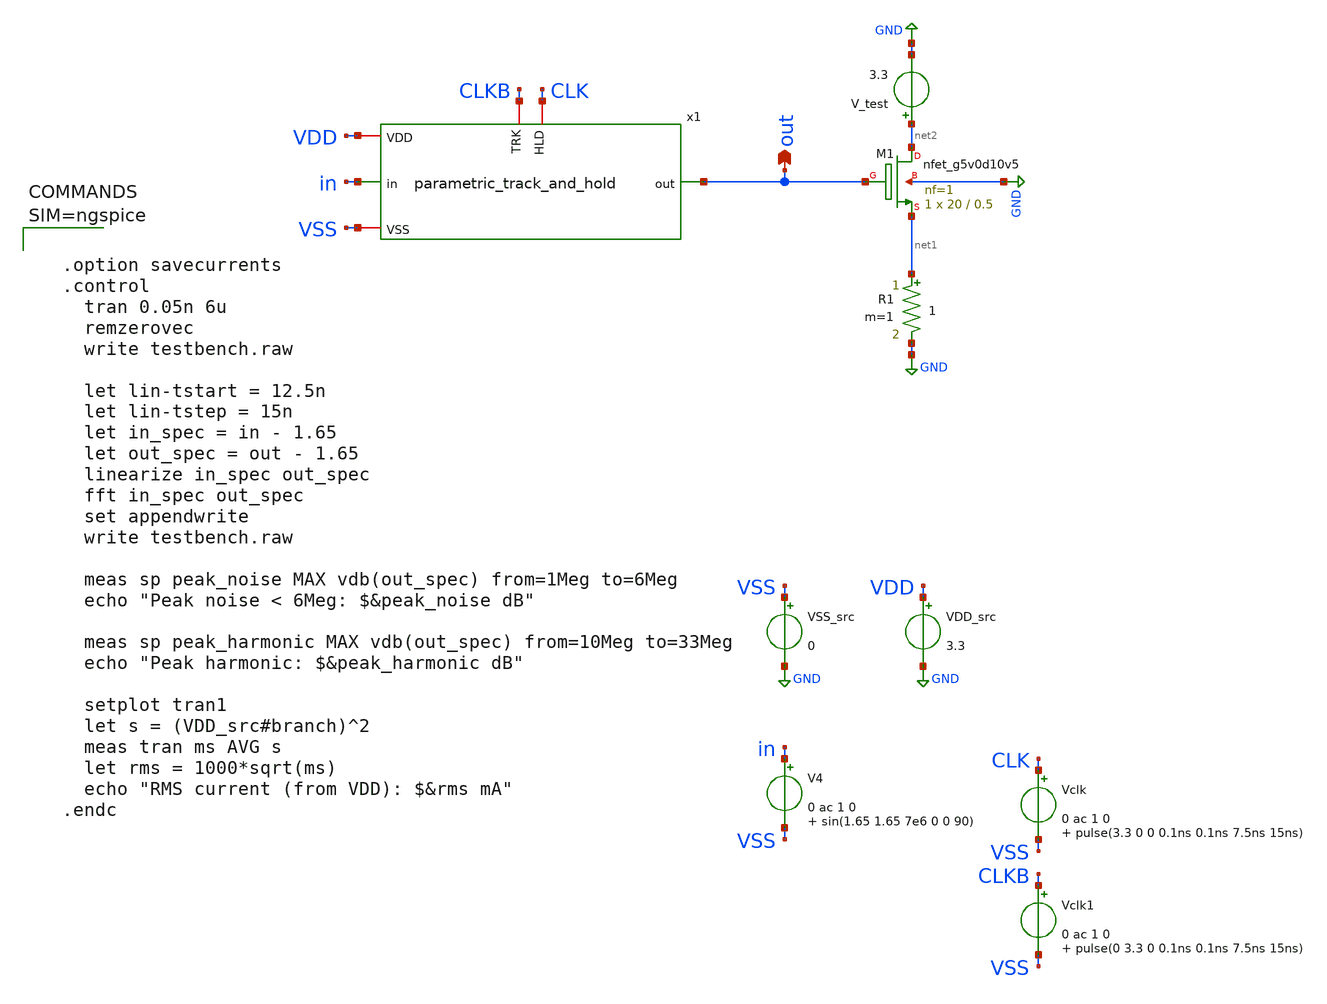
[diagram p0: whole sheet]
** sch_path: xschem/testbench.sch
**.subckt testbench out
*.opin out
VDD_src VDD GND 3.3
VSS_src VSS GND 0
V4 in VSS 0 ac 1 0 sin(1.65 1.65 7e6 0 0 90)
XM1 net2 out net1 GND sky130_fd_pr__nfet_g5v0d10v5 L=0.5 W=20 nf=1 ad='int((nf+1)/2) * W/nf * 0.29' as='int((nf+2)/2) * W/nf * 0.29'
+ pd='2*int((nf+1)/2) * (W/nf + 0.29)' ps='2*int((nf+2)/2) * (W/nf + 0.29)' nrd='0.29 / W' nrs='0.29 / W'
+ sa=0 sb=0 sd=0 mult=1 m=1
R1 net1 GND 1 m=1
Vclk CLK VSS 0 ac 1 0 pulse(3.3 0 0 0.1ns 0.1ns 7.5ns 15ns)
Vclk1 CLKB VSS 0 ac 1 0 pulse(0 3.3 0 0.1ns 0.1ns 7.5ns 15ns)
x1 CLK CLKB VDD VSS out in parametric_track_and_hold WT=1 PFT=1.21 PF=2 WS=5 WB=5 CB=18
V_test net2 GND 3.3
**** begin user architecture code

** opencircuitdesign pdks install
.lib $::SKYWATER_MODELS/sky130.lib.spice tt





  .option savecurrents
  .control
    tran 0.05n 6u
    remzerovec
    write testbench.raw

    let lin-tstart = 12.5n
    let lin-tstep = 15n
    let in_spec = in - 1.65
    let out_spec = out - 1.65
    linearize in_spec out_spec
    fft in_spec out_spec
    set appendwrite
    write testbench.raw

    meas sp peak_noise MAX vdb(out_spec) from=1Meg to=6Meg
    echo "Peak noise < 6Meg: $&peak_noise dB"

    meas sp peak_harmonic MAX vdb(out_spec) from=10Meg to=33Meg
    echo "Peak harmonic: $&peak_harmonic dB"

    setplot tran1
    let s = (VDD_src#branch)^2
    meas tran ms AVG s
    let rms = 1000*sqrt(ms)
    echo "RMS current (from VDD): $&rms mA"
  .endc



**** end user architecture code
**.ends

* expanding   symbol:  parametric_track_and_hold.sym # of pins=6
** sym_path: xschem/parametric_track_and_hold.sym
** sch_path: xschem/parametric_track_and_hold.sch
.subckt parametric_track_and_hold HLD TRK VDD VSS out in  WT=1 PFT=1.21 PF=2 WS=5 WB=5 CB=18
*.iopin VSS
*.iopin VDD
*.ipin in
*.opin out
*.iopin HLD
*.iopin TRK
XC2 out VSS sky130_fd_pr__cap_mim_m3_1 W=5 L=5 MF=1 m=1
XM1 out X in VSS sky130_fd_pr__nfet_g5v0d10v5 L=0.5 W={WT} nf=1 ad='int((nf+1)/2) * W/nf * 0.29' as='int((nf+2)/2) * W/nf * 0.29'
+ pd='2*int((nf+1)/2) * (W/nf + 0.29)' ps='2*int((nf+2)/2) * (W/nf + 0.29)' nrd='0.29 / W' nrs='0.29 / W'
+ sa=0 sb=0 sd=0 mult=1 m=1
XM1p out Xp in VDD sky130_fd_pr__pfet_g5v0d10v5 L=0.5 W={WT*PFT} nf=1 ad='int((nf+1)/2) * W/nf * 0.29'
+ as='int((nf+2)/2) * W/nf * 0.29' pd='2*int((nf+1)/2) * (W/nf + 0.29)' ps='2*int((nf+2)/2) * (W/nf + 0.29)'
+ nrd='0.29 / W' nrs='0.29 / W' sa=0 sb=0 sd=0 mult=1 m=1
XM4 net1 HLD VSS VSS sky130_fd_pr__nfet_g5v0d10v5 L=0.5 W={2*WS} nf=1 ad='int((nf+1)/2) * W/nf * 0.29'
+ as='int((nf+2)/2) * W/nf * 0.29' pd='2*int((nf+1)/2) * (W/nf + 0.29)' ps='2*int((nf+2)/2) * (W/nf + 0.29)'
+ nrd='0.29 / W' nrs='0.29 / W' sa=0 sb=0 sd=0 mult=1 m=1
XM2 P Y X P sky130_fd_pr__pfet_g5v0d10v5 L=0.5 W={WS*PF} nf=1 ad='int((nf+1)/2) * W/nf * 0.29' as='int((nf+2)/2) * W/nf * 0.29'
+ pd='2*int((nf+1)/2) * (W/nf + 0.29)' ps='2*int((nf+2)/2) * (W/nf + 0.29)' nrd='0.29 / W' nrs='0.29 / W'
+ sa=0 sb=0 sd=0 mult=1 m=1
XM3 in X Q VSS sky130_fd_pr__nfet_g5v0d10v5 L=0.5 W={WB} nf=1 ad='int((nf+1)/2) * W/nf * 0.29' as='int((nf+2)/2) * W/nf * 0.29'
+ pd='2*int((nf+1)/2) * (W/nf + 0.29)' ps='2*int((nf+2)/2) * (W/nf + 0.29)' nrd='0.29 / W' nrs='0.29 / W'
+ sa=0 sb=0 sd=0 mult=1 m=1
XM6 Q HLD VSS VSS sky130_fd_pr__nfet_g5v0d10v5 L=0.5 W={WB} nf=1 ad='int((nf+1)/2) * W/nf * 0.29' as='int((nf+2)/2) * W/nf * 0.29'
+ pd='2*int((nf+1)/2) * (W/nf + 0.29)' ps='2*int((nf+2)/2) * (W/nf + 0.29)' nrd='0.29 / W' nrs='0.29 / W'
+ sa=0 sb=0 sd=0 mult=1 m=1
XM3p Qp Xp in VDD sky130_fd_pr__pfet_g5v0d10v5 L=0.5 W={WB*PF} nf=1 ad='int((nf+1)/2) * W/nf * 0.29'
+ as='int((nf+2)/2) * W/nf * 0.29' pd='2*int((nf+1)/2) * (W/nf + 0.29)' ps='2*int((nf+2)/2) * (W/nf + 0.29)'
+ nrd='0.29 / W' nrs='0.29 / W' sa=0 sb=0 sd=0 mult=1 m=1
XM5 P X VDD P sky130_fd_pr__pfet_g5v0d10v5 L=0.5 W={WB*PF} nf=1 ad='int((nf+1)/2) * W/nf * 0.29' as='int((nf+2)/2) * W/nf * 0.29'
+ pd='2*int((nf+1)/2) * (W/nf + 0.29)' ps='2*int((nf+2)/2) * (W/nf + 0.29)' nrd='0.29 / W' nrs='0.29 / W'
+ sa=0 sb=0 sd=0 mult=1 m=1
XCb P Q sky130_fd_pr__cap_mim_m3_1 W={CB} L={CB} MF=1 m=1
XM8 X VDD net1 VSS sky130_fd_pr__nfet_g5v0d10v5 L=0.5 W={2*WS} nf=1 ad='int((nf+1)/2) * W/nf * 0.29'
+ as='int((nf+2)/2) * W/nf * 0.29' pd='2*int((nf+1)/2) * (W/nf + 0.29)' ps='2*int((nf+2)/2) * (W/nf + 0.29)'
+ nrd='0.29 / W' nrs='0.29 / W' sa=0 sb=0 sd=0 mult=1 m=1
XMb Y TRK VDD VDD sky130_fd_pr__pfet_g5v0d10v5 L=0.5 W={(WS/4)*PF} nf=1 ad='int((nf+1)/2) * W/nf * 0.29'
+ as='int((nf+2)/2) * W/nf * 0.29' pd='2*int((nf+1)/2) * (W/nf + 0.29)' ps='2*int((nf+2)/2) * (W/nf + 0.29)'
+ nrd='0.29 / W' nrs='0.29 / W' sa=0 sb=0 sd=0 mult=1 m=1
XMa Y TRK Q VSS sky130_fd_pr__nfet_g5v0d10v5 L=0.5 W={WS/10} nf=1 ad='int((nf+1)/2) * W/nf * 0.29' as='int((nf+2)/2) * W/nf * 0.29'
+ pd='2*int((nf+1)/2) * (W/nf + 0.29)' ps='2*int((nf+2)/2) * (W/nf + 0.29)' nrd='0.29 / W' nrs='0.29 / W'
+ sa=0 sb=0 sd=0 mult=1 m=1
XMc Q X Y VSS sky130_fd_pr__nfet_g5v0d10v5 L=0.5 W={WS} nf=1 ad='int((nf+1)/2) * W/nf * 0.29' as='int((nf+2)/2) * W/nf * 0.29'
+ pd='2*int((nf+1)/2) * (W/nf + 0.29)' ps='2*int((nf+2)/2) * (W/nf + 0.29)' nrd='0.29 / W' nrs='0.29 / W'
+ sa=0 sb=0 sd=0 mult=1 m=1
XCbp Pp Qp sky130_fd_pr__cap_mim_m3_1 W={CB} L={CB} MF=1 m=1
XM6p VDD TRK Qp VDD sky130_fd_pr__pfet_g5v0d10v5 L=0.5 W={WB*PF} nf=1 ad='int((nf+1)/2) * W/nf * 0.29'
+ as='int((nf+2)/2) * W/nf * 0.29' pd='2*int((nf+1)/2) * (W/nf + 0.29)' ps='2*int((nf+2)/2) * (W/nf + 0.29)'
+ nrd='0.29 / W' nrs='0.29 / W' sa=0 sb=0 sd=0 mult=1 m=1
XM5p VSS Xp Pp Pp sky130_fd_pr__nfet_g5v0d10v5 L=0.5 W={WB} nf=1 ad='int((nf+1)/2) * W/nf * 0.29' as='int((nf+2)/2) * W/nf * 0.29'
+ pd='2*int((nf+1)/2) * (W/nf + 0.29)' ps='2*int((nf+2)/2) * (W/nf + 0.29)' nrd='0.29 / W' nrs='0.29 / W'
+ sa=0 sb=0 sd=0 mult=1 m=1
XM2p Xp net2 Pp Pp sky130_fd_pr__nfet_g5v0d10v5 L=0.5 W={WS} nf=1 ad='int((nf+1)/2) * W/nf * 0.29' as='int((nf+2)/2) * W/nf * 0.29'
+ pd='2*int((nf+1)/2) * (W/nf + 0.29)' ps='2*int((nf+2)/2) * (W/nf + 0.29)' nrd='0.29 / W' nrs='0.29 / W'
+ sa=0 sb=0 sd=0 mult=1 m=1
XMcp net2 Xp Qp VDD sky130_fd_pr__pfet_g5v0d10v5 L=0.5 W={WS*PF} nf=1 ad='int((nf+1)/2) * W/nf * 0.29'
+ as='int((nf+2)/2) * W/nf * 0.29' pd='2*int((nf+1)/2) * (W/nf + 0.29)' ps='2*int((nf+2)/2) * (W/nf + 0.29)'
+ nrd='0.29 / W' nrs='0.29 / W' sa=0 sb=0 sd=0 mult=1 m=1
XMap Qp HLD net2 VDD sky130_fd_pr__pfet_g5v0d10v5 L=0.5 W={(WS/10)*PF} nf=1 ad='int((nf+1)/2) * W/nf * 0.29'
+ as='int((nf+2)/2) * W/nf * 0.29' pd='2*int((nf+1)/2) * (W/nf + 0.29)' ps='2*int((nf+2)/2) * (W/nf + 0.29)'
+ nrd='0.29 / W' nrs='0.29 / W' sa=0 sb=0 sd=0 mult=1 m=1
XMbp VSS HLD net2 VSS sky130_fd_pr__nfet_g5v0d10v5 L=0.5 W={WS/4} nf=1 ad='int((nf+1)/2) * W/nf * 0.29'
+ as='int((nf+2)/2) * W/nf * 0.29' pd='2*int((nf+1)/2) * (W/nf + 0.29)' ps='2*int((nf+2)/2) * (W/nf + 0.29)'
+ nrd='0.29 / W' nrs='0.29 / W' sa=0 sb=0 sd=0 mult=1 m=1
XM8p net3 VSS Xp VDD sky130_fd_pr__pfet_g5v0d10v5 L=0.5 W={2*WS*PF} nf=1 ad='int((nf+1)/2) * W/nf * 0.29'
+ as='int((nf+2)/2) * W/nf * 0.29' pd='2*int((nf+1)/2) * (W/nf + 0.29)' ps='2*int((nf+2)/2) * (W/nf + 0.29)'
+ nrd='0.29 / W' nrs='0.29 / W' sa=0 sb=0 sd=0 mult=1 m=1
XM4p VDD TRK net3 VDD sky130_fd_pr__pfet_g5v0d10v5 L=0.5 W={2*WS*PF} nf=1 ad='int((nf+1)/2) * W/nf * 0.29'
+ as='int((nf+2)/2) * W/nf * 0.29' pd='2*int((nf+1)/2) * (W/nf + 0.29)' ps='2*int((nf+2)/2) * (W/nf + 0.29)'
+ nrd='0.29 / W' nrs='0.29 / W' sa=0 sb=0 sd=0 mult=1 m=1
.ends

.GLOBAL GND
.end
